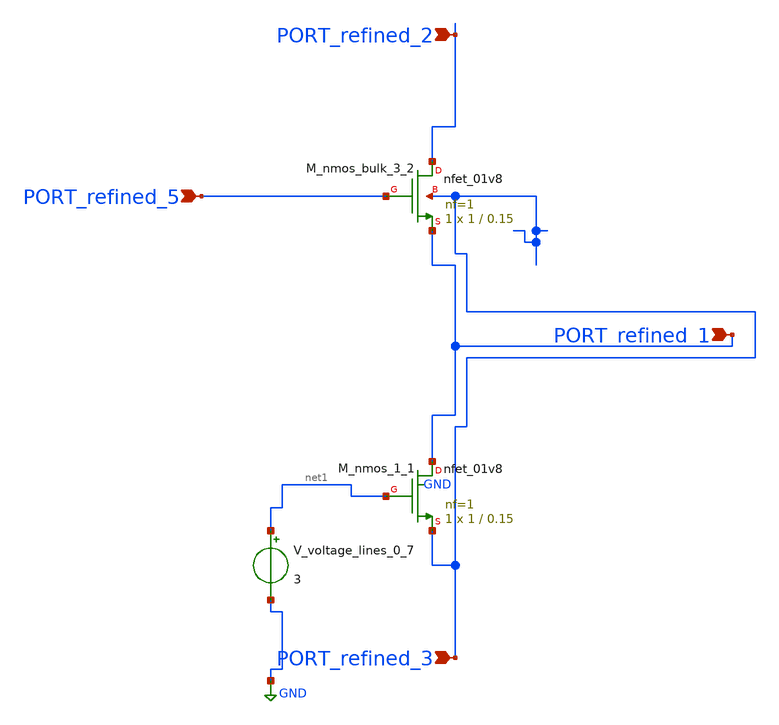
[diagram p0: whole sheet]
** sch_path: schematics/Image2Net/085.sch
**.subckt 085 PORT_refined_5 PORT_refined_1 PORT_refined_2 PORT_refined_3
*.ipin PORT_refined_5
*.ipin PORT_refined_1
*.ipin PORT_refined_2
*.ipin PORT_refined_3
XM_nmos_1_1 PORT_refined_1 net1 PORT_refined_3 GND sky130_fd_pr__nfet_01v8 L=0.15 W=1 nf=1 ad='int((1 + 1)/2) * 1 / 1 * 0.29'
+ as='int((1 + 2)/2) * 1 / 1 * 0.29' pd='2*int((1 + 1)/2) * (1 / 1 + 0.29)' ps='2*int((1 + 2)/2) * (1 / 1 + 0.29)'
+ nrd='0.29 / 1 ' nrs='0.29 / 1 ' sa=0 sb=0 sd=0 mult=1 m=1
XM_nmos_bulk_3_2 PORT_refined_2 PORT_refined_5 PORT_refined_1 PORT_refined_3 sky130_fd_pr__nfet_01v8
+ L=0.15 W=1 nf=1 ad='int((1 + 1)/2) * 1 / 1 * 0.29' as='int((1 + 2)/2) * 1 / 1 * 0.29' pd='2*int((1 + 1)/2) * (1 / 1 + 0.29)'
+ ps='2*int((1 + 2)/2) * (1 / 1 + 0.29)' nrd='0.29 / 1 ' nrs='0.29 / 1 ' sa=0 sb=0 sd=0 mult=1 m=1
V_voltage_lines_0_7 net1 GND 3
**.ends
.GLOBAL GND
.end
